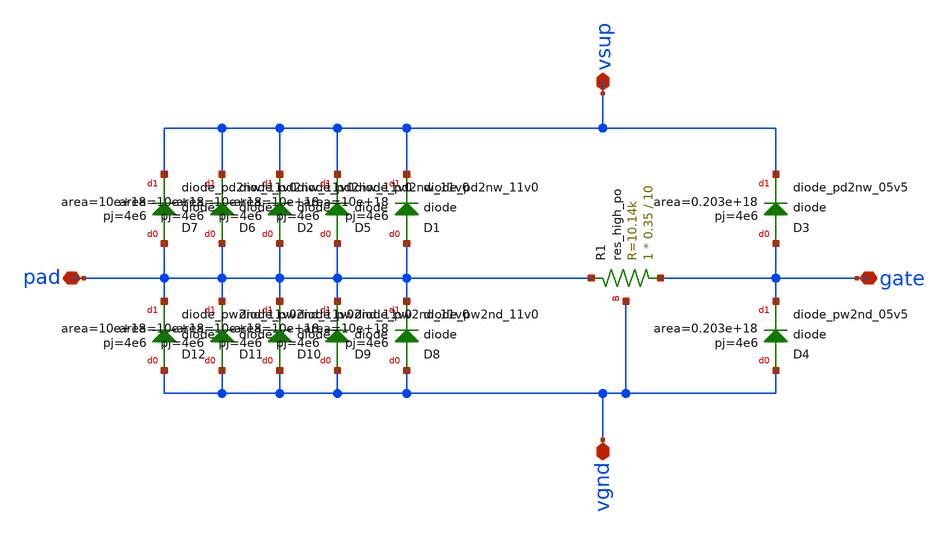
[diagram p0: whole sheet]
** sch_path: dev/esd_cell/tb/esd_cell.sch
**.subckt esd_cell vsup pad vgnd gate
*.iopin vsup
*.iopin pad
*.iopin vgnd
*.iopin gate
XD1 pad vsup sky130_fd_pr__diode_pd2nw_11v0 area=10e+18 pj=4e6
XD3 gate vsup sky130_fd_pr__diode_pd2nw_05v5 area=0.203e+18 pj=4e6
XD4 vgnd gate sky130_fd_pr__diode_pw2nd_05v5 area=0.203e+18 pj=4e6
XR1 gate pad vgnd sky130_fd_pr__res_high_po W=0.35 L=10 mult=1 m=1
XD8 vgnd pad sky130_fd_pr__diode_pw2nd_11v0 area=10e+18 pj=4e6
XD2 pad vsup sky130_fd_pr__diode_pd2nw_11v0 area=10e+18 pj=4e6
XD5 pad vsup sky130_fd_pr__diode_pd2nw_11v0 area=10e+18 pj=4e6
XD6 pad vsup sky130_fd_pr__diode_pd2nw_11v0 area=10e+18 pj=4e6
XD7 pad vsup sky130_fd_pr__diode_pd2nw_11v0 area=10e+18 pj=4e6
XD9 vgnd pad sky130_fd_pr__diode_pw2nd_11v0 area=10e+18 pj=4e6
XD10 vgnd pad sky130_fd_pr__diode_pw2nd_11v0 area=10e+18 pj=4e6
XD11 vgnd pad sky130_fd_pr__diode_pw2nd_11v0 area=10e+18 pj=4e6
XD12 vgnd pad sky130_fd_pr__diode_pw2nd_11v0 area=10e+18 pj=4e6
**.ends
.end
